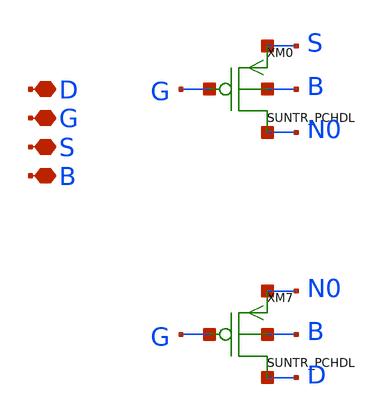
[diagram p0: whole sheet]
** sch_path: design/SUN_TR_SKY130NM/SUNTR_PCHDLCM.sch
**.subckt SUNTR_PCHDLCM D G S B
*.iopin D
*.iopin G
*.iopin S
*.iopin B
XM0 N0 G S B SUNTR_PCHDL
XM7 D G N0 B SUNTR_PCHDL
**.ends
.end
